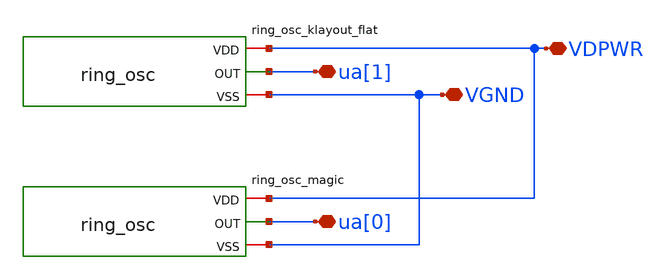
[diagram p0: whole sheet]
** sch_path: schem/tt_um_essen.sch
**.subckt tt_um_essen VDPWR VGND ua[1] ua[0]
*.iopin VDPWR
*.iopin VGND
*.iopin ua[1]
*.iopin ua[0]
ring_osc_klayout_flat VDPWR ua[1] VGND ring_osc
ring_osc_magic VDPWR ua[0] VGND ring_osc
**.ends

* expanding   symbol:  /foss/designs/analog/schem/ring_osc.sym # of pins=3
** sym_path: schem/ring_osc.sym
** sch_path: schem/ring_osc.sch
.subckt ring_osc VDD OUT VSS
*.iopin VDD
*.iopin VSS
*.opin OUT
x1 VDD OUT net1 VSS inv_cap
x2 VDD net1 net3 VSS inv_cap
x3 VDD net3 net2 VSS inv_cap
x4 VDD net2 net6 VSS inv_cap
x5 VDD net6 net4 VSS inv_cap
x6 VDD net4 net5 VSS inv_cap
x7 VDD net5 OUT VSS inv_cap
.ends


* expanding   symbol:  /foss/designs/sym/inv_cap.sym # of pins=4
** sym_path: schem/inv_cap.sym
** sch_path: schem/inv_cap.sch
.subckt inv_cap VDD A X VSS
*.ipin A
*.opin X
*.iopin VDD
*.iopin VSS
XM1 X A VDD VDD sky130_fd_pr__pfet_01v8_hvt L=1.0 W=2.0 nf=1 ad='int((1 + 1)/2) * 2.0 / 1 * 0.29' as='int((1 + 2)/2) * 2.0 / 1 * 0.29'
+ pd='2*int((1 + 1)/2) * (2.0 / 1 + 0.29)' ps='2*int((1 + 2)/2) * (2.0 / 1 + 0.29)' nrd='0.29 / 2.0 ' nrs='0.29 / 2.0 '
+ sa=0 sb=0 sd=0 mult=1 m=1
XM2 X A VSS GND sky130_fd_pr__nfet_01v8 L=1 W=1 nf=1 ad='int((1 + 1)/2) * 1 / 1 * 0.29' as='int((1 + 2)/2) * 1 / 1 * 0.29'
+ pd='2*int((1 + 1)/2) * (1 / 1 + 0.29)' ps='2*int((1 + 2)/2) * (1 / 1 + 0.29)' nrd='0.29 / 1 ' nrs='0.29 / 1 '
+ sa=0 sb=0 sd=0 mult=1 m=1
XC1 X VSS sky130_fd_pr__cap_mim_m3_1 W=6 L=5 MF=1 m=1
.ends

.end
